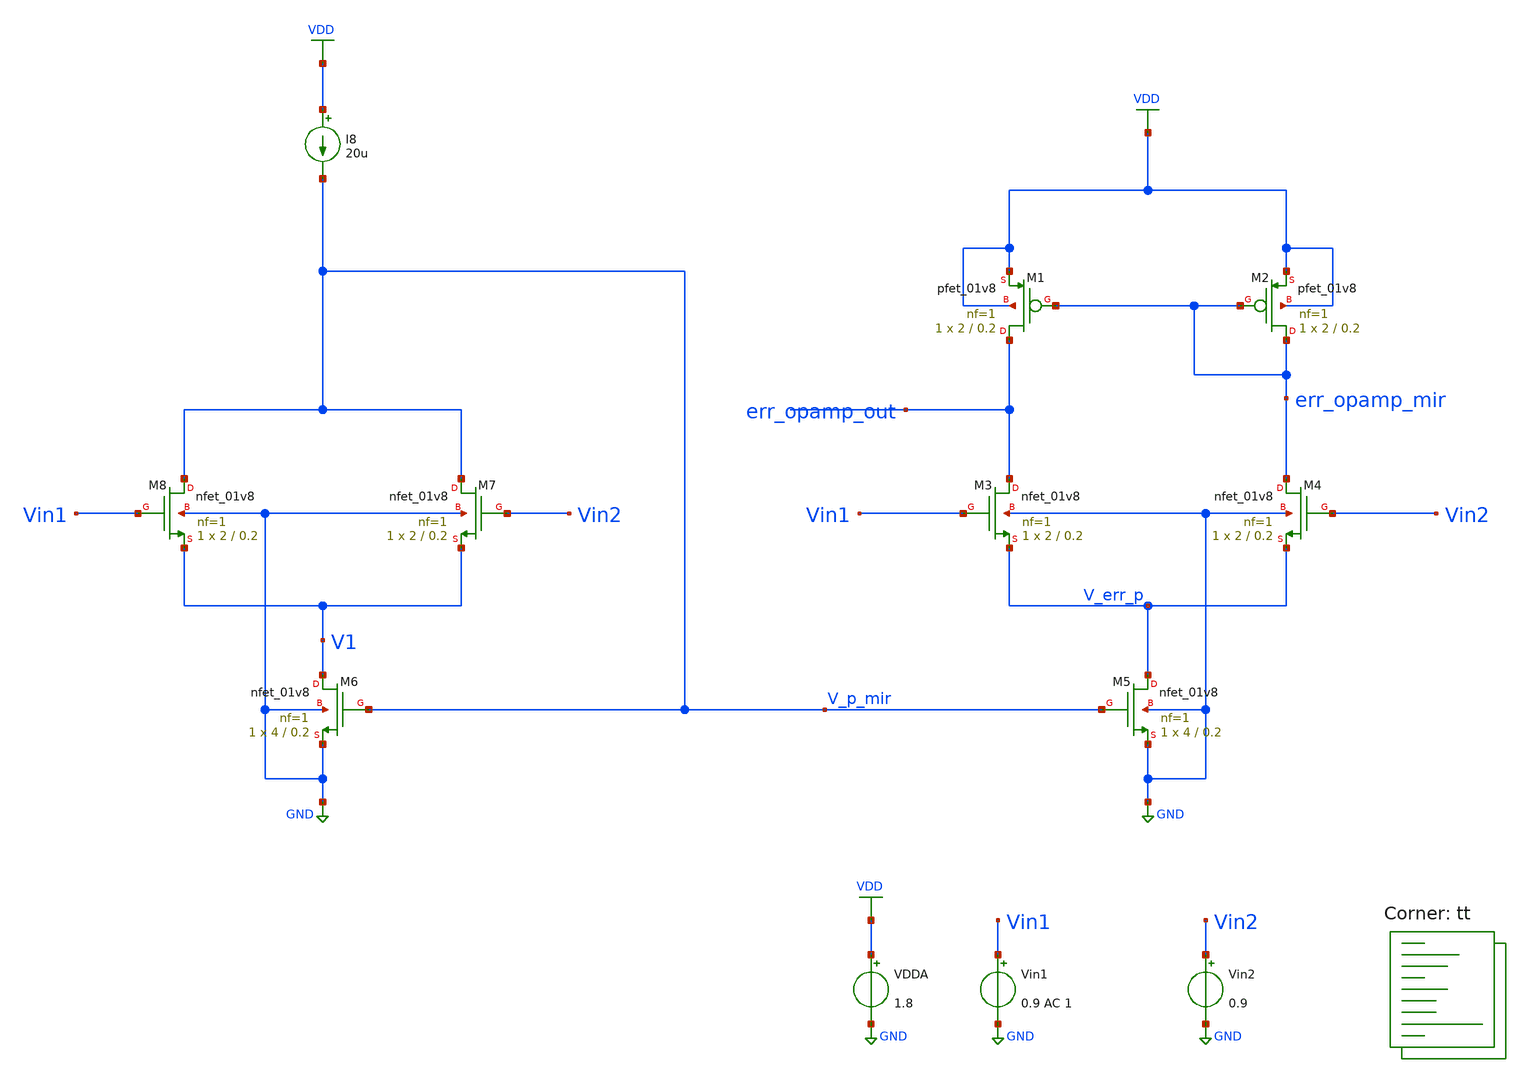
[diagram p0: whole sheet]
** sch_path: projects/opamp/xschem_ngspice/tb_opamp_2.sch
**.subckt tb_opamp_2
VDDA VDD GND 1.8
Vin1 Vin1 GND 0.9 AC 1
Vin2 Vin2 GND 0.9
XM2 err_opamp_mir err_opamp_mir VDD VDD sky130_fd_pr__pfet_01v8 L=0.2 W=2 nf=1 ad='int((nf+1)/2) * W/nf * 0.29'
+ as='int((nf+2)/2) * W/nf * 0.29' pd='2*int((nf+1)/2) * (W/nf + 0.29)' ps='2*int((nf+2)/2) * (W/nf + 0.29)'
+ nrd='0.29 / W' nrs='0.29 / W' sa=0 sb=0 sd=0 mult=1 m=1
XM1 err_opamp_out err_opamp_mir VDD VDD sky130_fd_pr__pfet_01v8 L=0.2 W=2 nf=1 ad='int((nf+1)/2) * W/nf * 0.29'
+ as='int((nf+2)/2) * W/nf * 0.29' pd='2*int((nf+1)/2) * (W/nf + 0.29)' ps='2*int((nf+2)/2) * (W/nf + 0.29)'
+ nrd='0.29 / W' nrs='0.29 / W' sa=0 sb=0 sd=0 mult=1 m=1
I8 VDD V_p_mir 20u
XM4 err_opamp_mir Vin2 V_err_p GND sky130_fd_pr__nfet_01v8 L=0.2 W=2 nf=1 ad='int((nf+1)/2) * W/nf * 0.29'
+ as='int((nf+2)/2) * W/nf * 0.29' pd='2*int((nf+1)/2) * (W/nf + 0.29)' ps='2*int((nf+2)/2) * (W/nf + 0.29)'
+ nrd='0.29 / W' nrs='0.29 / W' sa=0 sb=0 sd=0 mult=1 m=1
XM3 err_opamp_out Vin1 V_err_p GND sky130_fd_pr__nfet_01v8 L=0.2 W=2 nf=1 ad='int((nf+1)/2) * W/nf * 0.29'
+ as='int((nf+2)/2) * W/nf * 0.29' pd='2*int((nf+1)/2) * (W/nf + 0.29)' ps='2*int((nf+2)/2) * (W/nf + 0.29)'
+ nrd='0.29 / W' nrs='0.29 / W' sa=0 sb=0 sd=0 mult=1 m=1
XM5 V_err_p V_p_mir GND GND sky130_fd_pr__nfet_01v8 L=0.2 W=4 nf=1 ad='int((nf+1)/2) * W/nf * 0.29' as='int((nf+2)/2) * W/nf * 0.29'
+ pd='2*int((nf+1)/2) * (W/nf + 0.29)' ps='2*int((nf+2)/2) * (W/nf + 0.29)' nrd='0.29 / W' nrs='0.29 / W'
+ sa=0 sb=0 sd=0 mult=1 m=1
XM6 V1 V_p_mir GND GND sky130_fd_pr__nfet_01v8 L=0.2 W=4 nf=1 ad='int((nf+1)/2) * W/nf * 0.29' as='int((nf+2)/2) * W/nf * 0.29'
+ pd='2*int((nf+1)/2) * (W/nf + 0.29)' ps='2*int((nf+2)/2) * (W/nf + 0.29)' nrd='0.29 / W' nrs='0.29 / W'
+ sa=0 sb=0 sd=0 mult=1 m=1
XM7 V_p_mir Vin2 V1 GND sky130_fd_pr__nfet_01v8 L=0.2 W=2 nf=1 ad='int((nf+1)/2) * W/nf * 0.29' as='int((nf+2)/2) * W/nf * 0.29'
+ pd='2*int((nf+1)/2) * (W/nf + 0.29)' ps='2*int((nf+2)/2) * (W/nf + 0.29)' nrd='0.29 / W' nrs='0.29 / W'
+ sa=0 sb=0 sd=0 mult=1 m=1
XM8 V_p_mir Vin1 V1 GND sky130_fd_pr__nfet_01v8 L=0.2 W=2 nf=1 ad='int((nf+1)/2) * W/nf * 0.29' as='int((nf+2)/2) * W/nf * 0.29'
+ pd='2*int((nf+1)/2) * (W/nf + 0.29)' ps='2*int((nf+2)/2) * (W/nf + 0.29)' nrd='0.29 / W' nrs='0.29 / W'
+ sa=0 sb=0 sd=0 mult=1 m=1
**** begin user architecture code
.lib $::SKYWATER_MODELS/sky130.lib.spice tt



.option wnflag=1
.option savecurrents

* .param VDDGAUSS = agauss(1.8, 0.05, 1)
* .param VDD = VDDGAUSS
* .param VDD = 1.8

* .param TEMPGAUSS = agauss(40, 30, 1)
* .param temp = TEMPGAUSS
* .option temp = 26

.save @m.xm1.msky130_fd_pr__pfet_01v8[gm] @m.xm1.msky130_fd_pr__pfet_01v8[vds] @m.xm1.msky130_fd_pr__pfet_01v8[vth] @m.xm2.msky130_fd_pr__pfet_01v8[gm] @m.xm2.msky130_fd_pr__pfet_01v8[vds] @m.xm2.msky130_fd_pr__pfet_01v8[vth] @m.xm3.msky130_fd_pr__nfet_01v8[gm] @m.xm3.msky130_fd_pr__nfet_01v8[vds] @m.xm3.msky130_fd_pr__nfet_01v8[vth] @m.xm4.msky130_fd_pr__nfet_01v8[gm] @m.xm4.msky130_fd_pr__nfet_01v8[vds] @m.xm4.msky130_fd_pr__nfet_01v8[vth] @m.xm5.msky130_fd_pr__nfet_01v8[gm] @m.xm5.msky130_fd_pr__nfet_01v8[vds] @m.xm5.msky130_fd_pr__nfet_01v8[vth] @m.xm6.msky130_fd_pr__nfet_01v8[gm] @m.xm6.msky130_fd_pr__nfet_01v8[vds] @m.xm6.msky130_fd_pr__nfet_01v8[vth] @m.xm7.msky130_fd_pr__nfet_01v8[gm] @m.xm7.msky130_fd_pr__nfet_01v8[vds] @m.xm7.msky130_fd_pr__nfet_01v8[vth] @m.xm8.msky130_fd_pr__nfet_01v8[gm] @m.xm8.msky130_fd_pr__nfet_01v8[vds] @m.xm8.msky130_fd_pr__nfet_01v8[vth]

.control

  save all
  * tran 1u 20m
  ac dec 20 1 1T
  let rout=deriv(@m.xm2.msky130_fd_pr__pfet_01v8[vds])/deriv(@m.xm2.msky130_fd_pr__pfet_01v8[id])
  write tb_opamp_2.raw
  set appendwrite
  show
  * let a = deriv(@m.xm2.msky130_fd_pr__pfet_01v8[vds])
  * let b = deriv(@m.xm2.msky130_fd_pr__pfet_01v8[id])
  * plot deriv(@m.xm2.msky130_fd_pr__pfet_01v8[vds])/deriv(@m.xm2.msky130_fd_pr__pfet_01v8[id])
  * plot rout
  * plot a
.endc




**** end user architecture code
**.ends
.GLOBAL GND
.GLOBAL VDD
.end
